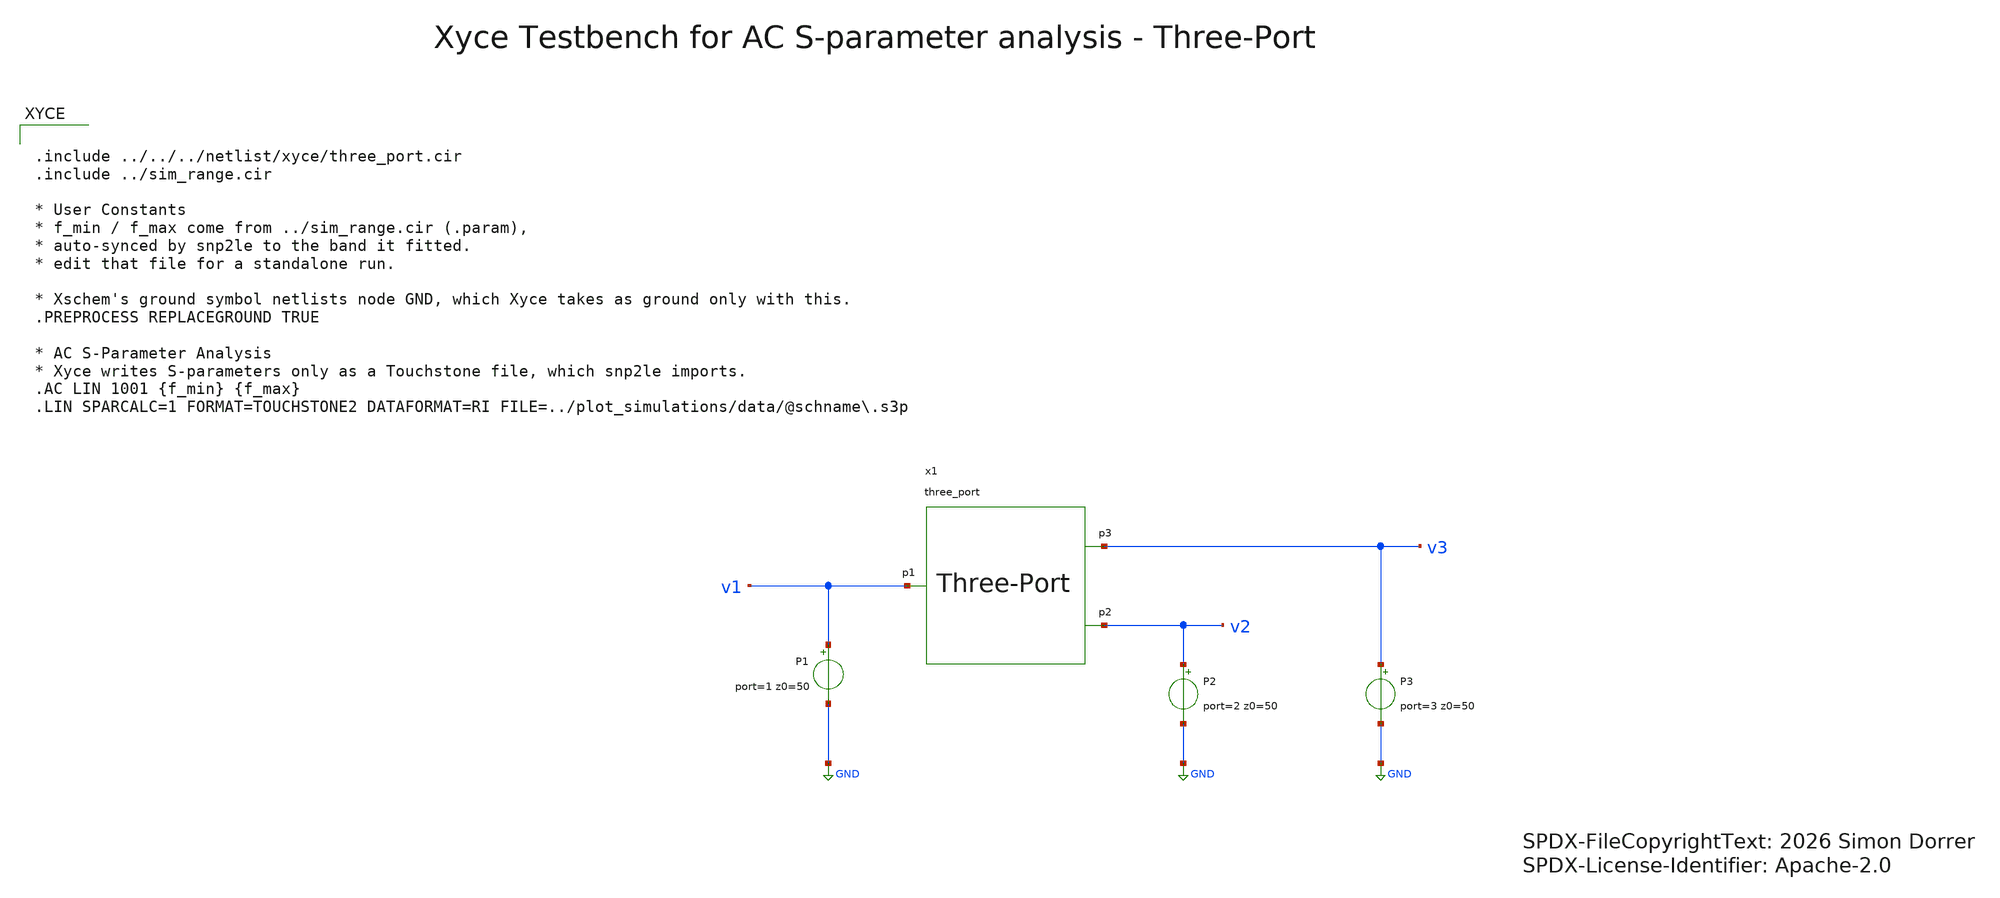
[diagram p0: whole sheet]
** sch_path: testbenches/xschem/three_port_tb_acsp_xyce.sch
* SPDX-FileCopyrightText: 2026 Simon Dorrer
* SPDX-License-Identifier: Apache-2.0
**.subckt three_port_tb_acsp_xyce
P1 v1 GND port=1 z0=50
P2 v2 GND port=2 z0=50
x1 v1 v2 v3 three_port
P3 v3 GND port=3 z0=50
**** begin user architecture code


.include ../../../netlist/xyce/three_port.cir
.include ../sim_range.cir

* User Constants
* f_min / f_max come from ../sim_range.cir (.param),
* auto-synced by snp2le to the band it fitted.
* edit that file for a standalone run.

* Xschem's ground symbol netlists node GND, which Xyce takes as ground only with this.
.PREPROCESS REPLACEGROUND TRUE

* AC S-Parameter Analysis
* Xyce writes S-parameters only as a Touchstone file, which snp2le imports.
.AC LIN 1001 {f_min} {f_max}
.LIN SPARCALC=1 FORMAT=TOUCHSTONE2 DATAFORMAT=RI FILE=../plot_simulations/data/@schname\.s3p


**** end user architecture code
**.ends
.GLOBAL GND
.end
